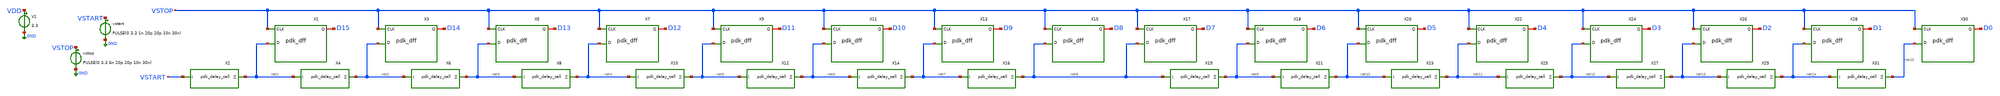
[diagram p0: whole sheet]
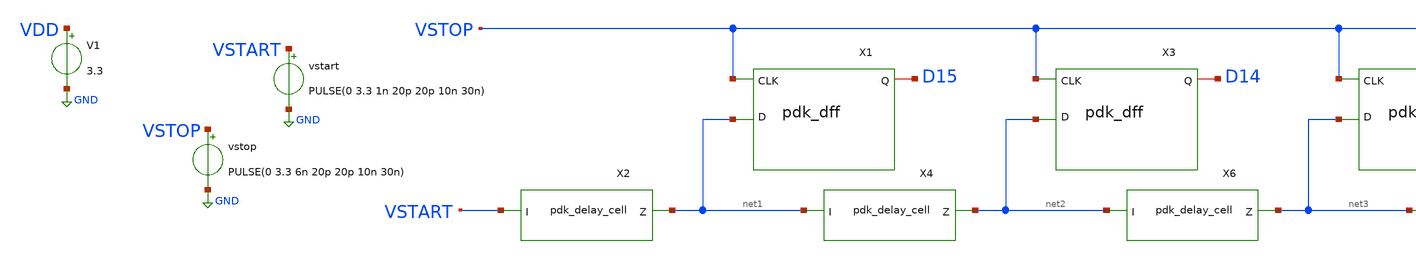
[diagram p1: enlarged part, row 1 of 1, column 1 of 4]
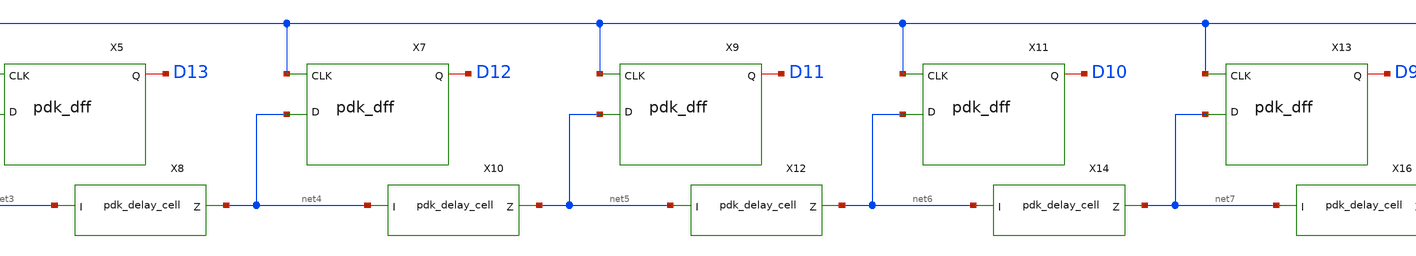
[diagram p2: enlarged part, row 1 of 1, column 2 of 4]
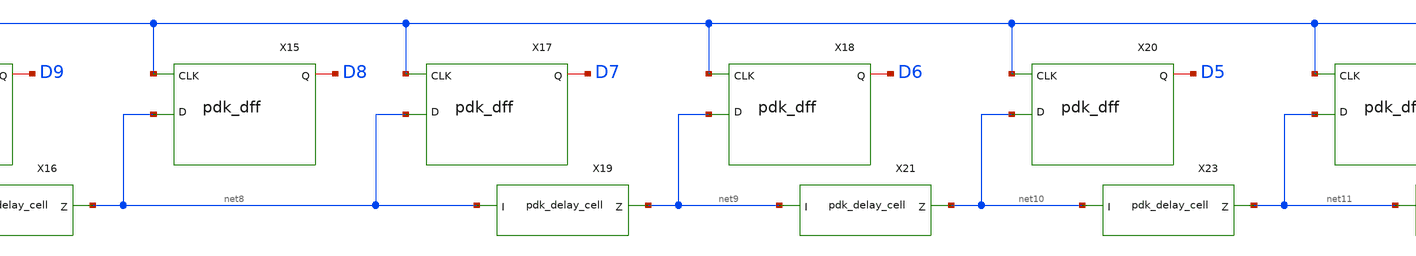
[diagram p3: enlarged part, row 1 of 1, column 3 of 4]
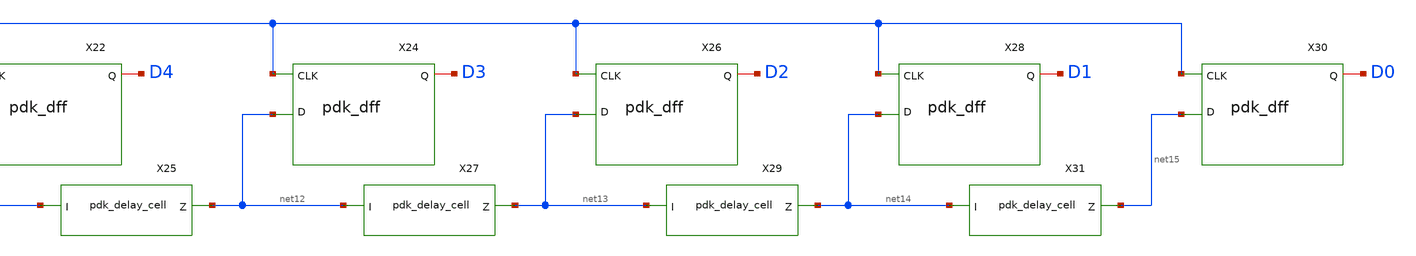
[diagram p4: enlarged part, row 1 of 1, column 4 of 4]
** sch_path: schem/medium_delay_line_test.sch
**.subckt medium_delay_line_test
X1 net1 VSTOP D15 VDD VDD 0 0 gf180mcu_fd_sc_mcu7t5v0__dffq_4
X2 VSTART net1 VDD VDD 0 0 gf180mcu_fd_sc_mcu7t5v0__dlyc_1
X3 net2 VSTOP D14 VDD VDD 0 0 gf180mcu_fd_sc_mcu7t5v0__dffq_4
X4 net1 net2 VDD VDD 0 0 gf180mcu_fd_sc_mcu7t5v0__dlyc_1
X5 net3 VSTOP D13 VDD VDD 0 0 gf180mcu_fd_sc_mcu7t5v0__dffq_4
X6 net2 net3 VDD VDD 0 0 gf180mcu_fd_sc_mcu7t5v0__dlyc_1
X7 net4 VSTOP D12 VDD VDD 0 0 gf180mcu_fd_sc_mcu7t5v0__dffq_4
X8 net3 net4 VDD VDD 0 0 gf180mcu_fd_sc_mcu7t5v0__dlyc_1
X9 net5 VSTOP D11 VDD VDD 0 0 gf180mcu_fd_sc_mcu7t5v0__dffq_4
X10 net4 net5 VDD VDD 0 0 gf180mcu_fd_sc_mcu7t5v0__dlyc_1
X11 net6 VSTOP D10 VDD VDD 0 0 gf180mcu_fd_sc_mcu7t5v0__dffq_4
X12 net5 net6 VDD VDD 0 0 gf180mcu_fd_sc_mcu7t5v0__dlyc_1
X13 net7 VSTOP D9 VDD VDD 0 0 gf180mcu_fd_sc_mcu7t5v0__dffq_4
X14 net6 net7 VDD VDD 0 0 gf180mcu_fd_sc_mcu7t5v0__dlyc_1
X15 net8 VSTOP D8 VDD VDD 0 0 gf180mcu_fd_sc_mcu7t5v0__dffq_4
X16 net7 net8 VDD VDD 0 0 gf180mcu_fd_sc_mcu7t5v0__dlyc_1
vstart VSTART GND PULSE(0 3.3 1n 20p 20p 10n 30n)
vstop VSTOP GND PULSE(0 3.3 6n 20p 20p 10n 30n)
V1 VDD GND 3.3
X17 net8 VSTOP D7 VDD VDD 0 0 gf180mcu_fd_sc_mcu7t5v0__dffq_4
X18 net9 VSTOP D6 VDD VDD 0 0 gf180mcu_fd_sc_mcu7t5v0__dffq_4
X19 net8 net9 VDD VDD 0 0 gf180mcu_fd_sc_mcu7t5v0__dlyc_1
X20 net10 VSTOP D5 VDD VDD 0 0 gf180mcu_fd_sc_mcu7t5v0__dffq_4
X21 net9 net10 VDD VDD 0 0 gf180mcu_fd_sc_mcu7t5v0__dlyc_1
X22 net11 VSTOP D4 VDD VDD 0 0 gf180mcu_fd_sc_mcu7t5v0__dffq_4
X23 net10 net11 VDD VDD 0 0 gf180mcu_fd_sc_mcu7t5v0__dlyc_1
X24 net12 VSTOP D3 VDD VDD 0 0 gf180mcu_fd_sc_mcu7t5v0__dffq_4
X25 net11 net12 VDD VDD 0 0 gf180mcu_fd_sc_mcu7t5v0__dlyc_1
X26 net13 VSTOP D2 VDD VDD 0 0 gf180mcu_fd_sc_mcu7t5v0__dffq_4
X27 net12 net13 VDD VDD 0 0 gf180mcu_fd_sc_mcu7t5v0__dlyc_1
X28 net14 VSTOP D1 VDD VDD 0 0 gf180mcu_fd_sc_mcu7t5v0__dffq_4
X29 net13 net14 VDD VDD 0 0 gf180mcu_fd_sc_mcu7t5v0__dlyc_1
X30 net15 VSTOP D0 VDD VDD 0 0 gf180mcu_fd_sc_mcu7t5v0__dffq_4
X31 net14 net15 VDD VDD 0 0 gf180mcu_fd_sc_mcu7t5v0__dlyc_1
**** begin user architecture code


.include /usr/local/share/pdk/gf180mcuD/libs.tech/ngspice/design.ngspice
.lib /usr/local/share/pdk/gf180mcuD/libs.tech/ngspice/sm141064.ngspice typical
.include /usr/local/share/pdk/gf180mcuD/libs.ref/gf180mcu_fd_sc_mcu7t5v0/spice/gf180mcu_fd_sc_mcu7t5v0.spice




.tran 1p 30n 0 1p

.meas tran b15 FIND v(d15) AT=8n
.meas tran b14 FIND v(d14) AT=8n
.meas tran b13 FIND v(d13) AT=8n
.meas tran b12 FIND v(d12) AT=8n
.meas tran b11 FIND v(d11) AT=8n
.meas tran b10 FIND v(d10) AT=8n
.meas tran b9 FIND v(d9) AT=8n
.meas tran b8 FIND v(d8) AT=8n
.meas tran b7 FIND v(d7) AT=8n
.meas tran b6 FIND v(d6) AT=8n
.meas tran b5 FIND v(d5) AT=8n
.meas tran b4 FIND v(d4) AT=8n
.meas tran b3 FIND v(d3) AT=8n
.meas tran b2 FIND v(d2) AT=8n
.meas tran b1 FIND v(d1) AT=8n
.meas tran b0 FIND v(d0) AT=8n

.meas tran t1 WHEN v(net1)=1.65 RISE=1
.meas tran t2 WHEN v(net2)=1.65 RISE=1
.meas tran t3 WHEN v(net3)=1.65 RISE=1

.meas tran bin1 PARAM='t2-t1'
.meas tran bin2 PARAM='t3-t2'


**** end user architecture code
**.ends
.GLOBAL GND
.end
